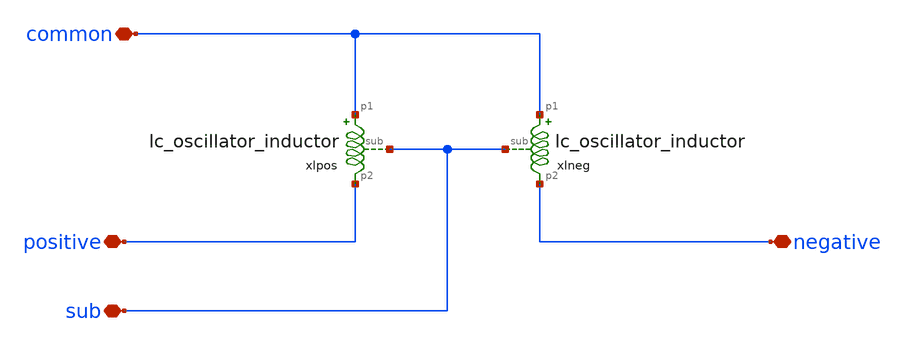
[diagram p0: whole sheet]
** sch_path: design/lc_oscillator_inductor_diff/lc_oscillator_inductor_diff.sch
**.subckt lc_oscillator_inductor_diff common positive sub negative
*.iopin common
*.iopin positive
*.iopin sub
*.iopin negative
xlneg common negative sub lc_oscillator_inductor
xlpos common positive sub lc_oscillator_inductor
**.ends

* expanding   symbol:  lc_oscillator_inductor/lc_oscillator_inductor.sym # of pins=3
** sym_path: design/lc_oscillator_inductor/lc_oscillator_inductor.sym
** sch_path: design/lc_oscillator_inductor/lc_oscillator_inductor.sch
.subckt lc_oscillator_inductor p1 p2 sub
*.iopin p2
*.iopin p1
*.iopin sub
L1 net1 p1 1.028n m=1
C1 p1 net2 62.02f m=1
R1 net2 sub 16.03 m=1
C2 p1 p2 0.1f m=1
C3 p2 net3 62.31f m=1
R2 net3 sub 15.88 m=1
R3 p2 net1 3.6825 m=1
.ends

.end
